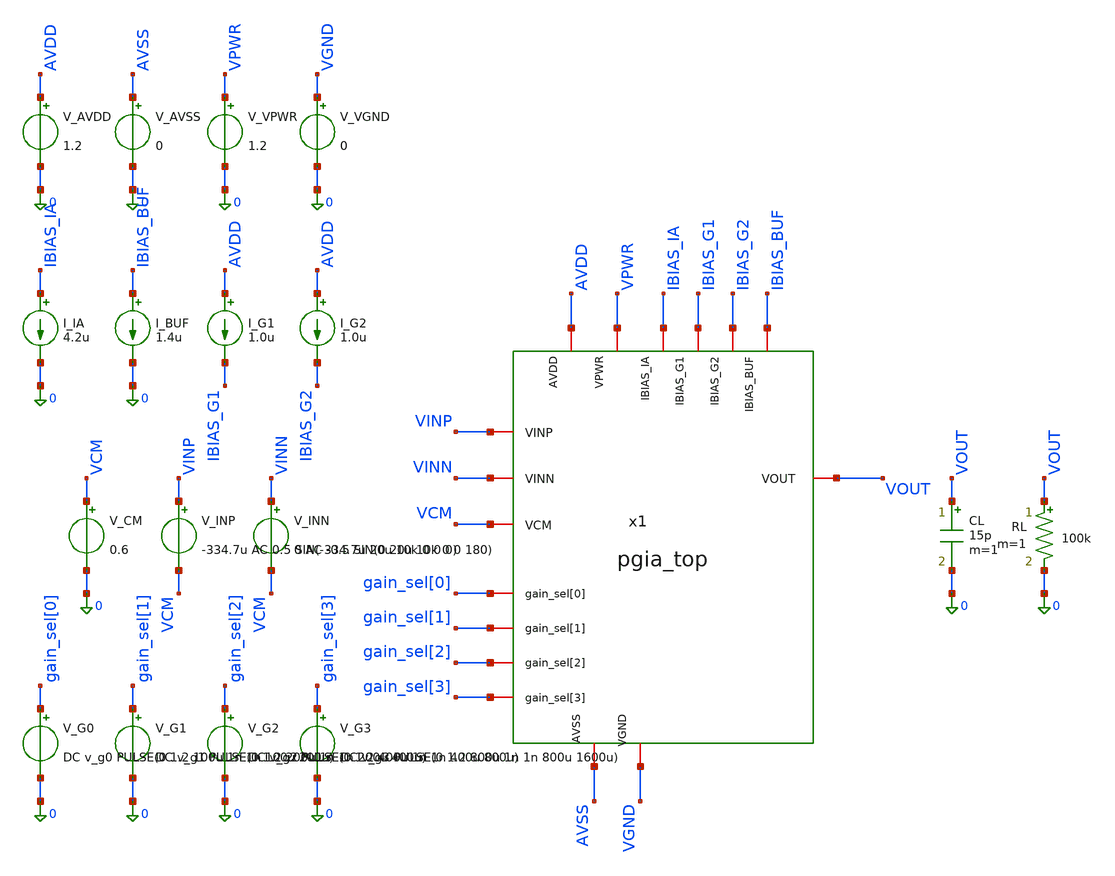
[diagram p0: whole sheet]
** sch_path: xschem/pgia_top/tb_pgia_top.sch
**.subckt tb_pgia_top
x1 VINP VINN VCM gain_sel[0] gain_sel[1] gain_sel[2] gain_sel[3] VOUT AVDD VPWR IBIAS_IA IBIAS_G1
+ IBIAS_G2 IBIAS_BUF AVSS VGND pgia_top
V_AVDD AVDD 0 1.2
V_AVSS AVSS 0 0
V_VPWR VPWR 0 1.2
V_VGND VGND 0 0
I_IA IBIAS_IA 0 4.2u
I_BUF IBIAS_BUF 0 1.4u
I_G1 AVDD IBIAS_G1 1.0u
I_G2 AVDD IBIAS_G2 1.0u
V_CM VCM 0 0.6
V_INP VINP VCM -334.7u AC 0.5 SIN(-334.7u 20u 10k 0 0 0)
V_INN VINN VCM 0 AC -0.5 SIN(0 20u 10k 0 0 180)
V_G0 gain_sel[0] 0 DC v_g0 PULSE(0 1.2 100u 1n 1n 100u 200u)
V_G1 gain_sel[1] 0 DC v_g1 PULSE(0 1.2 200u 1n 1n 200u 400u)
V_G2 gain_sel[2] 0 DC v_g2 PULSE(0 1.2 400u 1n 1n 400u 800u)
V_G3 gain_sel[3] 0 DC v_g3 PULSE(0 1.2 800u 1n 1n 800u 1600u)
CL VOUT 0 15p m=1
RL VOUT 0 100k m=1
**** begin user architecture code


.lib /foss/pdks/ihp-sg13cmos5l/libs.tech/ngspice/models/cornerMOSlv.lib mos_tt
.lib /foss/pdks/ihp-sg13cmos5l/libs.tech/ngspice/models/cornerRES.lib res_typ
.lib /foss/pdks/ihp-sg13cmos5l/libs.tech/ngspice/models/cornerCAP.lib cap_typ
.include /foss/pdks/ihp-sg13cmos5l/libs.ref/sg13cmos5l_stdcell/spice/sg13cmos5l_stdcell.spice
.include /foss/designs/Chipalooza/Programmable-Instrumentation-Amplifier-IP/gds/gain_decoder_4b/final/spice/gain_decoder_4b.spice

.param temp=27
.param lbias=0.15u wbias=0.15u
.param m6=1 m7=4 m8=8
.param linpair=3u winpair=20u
.param lload=5u wload=10u
.param lcs=3u wcs=20u
.param Cc=2p
.param v_g0=0 v_g1=0 v_g2=0 v_g3=0




.control
  save all v(VOUT) v(x1.v_ia) v(x1.v_stage1) v(x1.v_stage2)
  echo ==========================================================================
  echo === TOP-LEVEL PGIA CO-SIMULATION BATTERY (MILESTONES 3, 4, 5) ===
  echo ==========================================================================

  * 1. DC Operating Point Verification
  echo
  echo --- Phase A: DC Operating Point Audit ---
  op
  let v_ia_dc     = v(x1.v_ia)
  let v_st1_dc    = v(x1.v_stage1)
  let v_st2_dc    = v(x1.v_stage2)
  let v_out_dc    = v(VOUT)
  let v_diff_dc   = v(VINP) - v(VINN)
  let i_avdd_dc   = -i(v_avdd)
  let i_vpwr_dc   = -i(v_vpwr)
  let p_tot_uW    = (i_avdd_dc + i_vpwr_dc) * 1.2 * 1e6

  echo Target Common-Mode: 0.600 V
  echo V(VINP) - V(VINN) = $&v_diff_dc V
  echo V(v_ia)           = $&v_ia_dc V
  echo V(v_stage1)       = $&v_st1_dc V
  echo V(v_stage2)       = $&v_st2_dc V
  echo V(VOUT)           = $&v_out_dc V
  echo Total Static DC Power = $&p_tot_uW uW (Target < 500 uW)

  * 2. Small-Signal AC Gain Sweeps Across All 11 Valid Gain Steps (0 to 10)
  echo
  echo --- Phase B: Small-Signal AC Frequency Response (11 Steps) ---

  * Step 0: 0000 (Target: 18.06 dB / 8x)
  alterparam v_g0=0
  alterparam v_g1=0
  alterparam v_g2=0
  alterparam v_g3=0
  reset
  ac dec 10 10 100Meg
  let gain0 = db(v(VOUT))
  let g0_1k = gain0[20]
  echo Step 0  (0000): Gain @ 1kHz = $&g0_1k dB

  * Step 1: 0001 (Target: 24.08 dB / 16x)
  alterparam v_g0=1.2
  alterparam v_g1=0
  alterparam v_g2=0
  alterparam v_g3=0
  reset
  ac dec 10 10 100Meg
  let gain1 = db(v(VOUT))
  let g1_1k = gain1[20]
  echo Step 1  (0001): Gain @ 1kHz = $&g1_1k dB

  * Step 2: 0010 (Target: 30.10 dB / 32x)
  alterparam v_g0=0
  alterparam v_g1=1.2
  alterparam v_g2=0
  alterparam v_g3=0
  reset
  ac dec 10 10 100Meg
  let gain2 = db(v(VOUT))
  let g2_1k = gain2[20]
  echo Step 2  (0010): Gain @ 1kHz = $&g2_1k dB

  * Step 3: 0011 (Target: 36.12 dB / 64x)
  alterparam v_g0=1.2
  alterparam v_g1=1.2
  alterparam v_g2=0
  alterparam v_g3=0
  reset
  ac dec 10 10 100Meg
  let gain3 = db(v(VOUT))
  let g3_1k = gain3[20]
  echo Step 3  (0011): Gain @ 1kHz = $&g3_1k dB

  * Step 4: 0100 (Target: 42.14 dB / 128x)
  alterparam v_g0=0
  alterparam v_g1=0
  alterparam v_g2=1.2
  alterparam v_g3=0
  reset
  ac dec 10 10 100Meg
  let gain4 = db(v(VOUT))
  let g4_1k = gain4[20]
  echo Step 4  (0100): Gain @ 1kHz = $&g4_1k dB

  * Step 5: 0101 (Target: 48.16 dB / 256x)
  alterparam v_g0=1.2
  alterparam v_g1=0
  alterparam v_g2=1.2
  alterparam v_g3=0
  reset
  ac dec 10 10 100Meg
  let gain5 = db(v(VOUT))
  let g5_1k = gain5[20]
  echo Step 5  (0101): Gain @ 1kHz = $&g5_1k dB

  * Step 6: 0110 (Target: 54.18 dB / 512x)
  alterparam v_g0=0
  alterparam v_g1=1.2
  alterparam v_g2=1.2
  alterparam v_g3=0
  reset
  ac dec 10 10 100Meg
  let gain6 = db(v(VOUT))
  let g6_1k = gain6[20]
  echo Step 6  (0110): Gain @ 1kHz = $&g6_1k dB

  * Step 7: 0111 (Target: 60.20 dB / 1024x)
  alterparam v_g0=1.2
  alterparam v_g1=1.2
  alterparam v_g2=1.2
  alterparam v_g3=0
  reset
  ac dec 10 10 100Meg
  let gain7 = db(v(VOUT))
  let g7_1k = gain7[20]
  echo Step 7  (0111): Gain @ 1kHz = $&g7_1k dB

  * Step 8: 1000 (Target: 66.22 dB / 2048x)
  alterparam v_g0=0
  alterparam v_g1=0
  alterparam v_g2=0
  alterparam v_g3=1.2
  reset
  ac dec 10 10 100Meg
  let gain8 = db(v(VOUT))
  let g8_1k = gain8[20]
  echo Step 8  (1000): Gain @ 1kHz = $&g8_1k dB

  * Step 9: 1001 (Target: 72.24 dB / 4096x)
  alterparam v_g0=1.2
  alterparam v_g1=0
  alterparam v_g2=0
  alterparam v_g3=1.2
  reset
  ac dec 10 10 100Meg
  let gain9 = db(v(VOUT))
  let g9_1k = gain9[20]
  echo Step 9  (1001): Gain @ 1kHz = $&g9_1k dB

  * Step 10: 1010 (Target: 78.26 dB / 8192x)
  alterparam v_g0=0
  alterparam v_g1=1.2
  alterparam v_g2=0
  alterparam v_g3=1.2
  reset
  ac dec 10 10 100Meg
  let gain10 = db(v(VOUT))
  let g10_1k = gain10[20]
  echo Step 10 (1010): Gain @ 1kHz = $&g10_1k dB

  * Step 11: 1011 (Out-of-range Clamp Target)
  alterparam v_g0=1.2
  alterparam v_g1=1.2
  alterparam v_g2=0
  alterparam v_g3=1.2
  reset
  ac dec 10 10 100Meg
  let gain11 = db(v(VOUT))
  let g11_1k = gain11[20]
  echo Step 11 (1011): Gain @ 1kHz = $&g11_1k dB (Expected Clamp to Step 0)

  * 3. Dynamic Transient Co-Simulation Across All 16 States (0 to 15)
  echo
  echo --- Phase C: Dynamic Transient Stepping (16 States x 100us) ---
  tran 1u 1.6m
  meas tran vpp_st0  pp v(VOUT) from=50u to=90u
  meas tran vpp_st1  pp v(VOUT) from=150u to=190u
  meas tran vpp_st2  pp v(VOUT) from=250u to=290u
  meas tran vpp_st3  pp v(VOUT) from=350u to=390u
  meas tran vpp_st4  pp v(VOUT) from=450u to=490u
  meas tran vpp_st5  pp v(VOUT) from=550u to=590u
  meas tran vpp_st6  pp v(VOUT) from=650u to=690u
  meas tran vpp_st7  pp v(VOUT) from=750u to=790u
  meas tran vpp_st8  pp v(VOUT) from=850u to=890u
  meas tran vpp_st9  pp v(VOUT) from=950u to=990u
  meas tran vpp_st10 pp v(VOUT) from=1050u to=1090u
  meas tran vpp_st11 pp v(VOUT) from=1150u to=1190u
  meas tran vpp_st12 pp v(VOUT) from=1250u to=1290u
  meas tran vpp_st15 pp v(VOUT) from=1550u to=1590u

  echo
  echo Transient Output Peak-to-Peak:
  echo State 0  (0000): $&vpp_st0 Vpp
  echo State 1  (0001): $&vpp_st1 Vpp
  echo State 2  (0010): $&vpp_st2 Vpp
  echo State 3  (0011): $&vpp_st3 Vpp
  echo State 4  (0100): $&vpp_st4 Vpp
  echo State 5  (0101): $&vpp_st5 Vpp
  echo State 6  (0110): $&vpp_st6 Vpp
  echo State 7  (0111): $&vpp_st7 Vpp
  echo State 8  (1000): $&vpp_st8 Vpp
  echo State 9  (1001): $&vpp_st9 Vpp
  echo State 10 (1010): $&vpp_st10 Vpp
  echo State 11 (1011): $&vpp_st11 Vpp (Clamped)
  echo State 12 (1100): $&vpp_st12 Vpp (Clamped)
  echo State 15 (1111): $&vpp_st15 Vpp (Clamped)

  echo ==========================================================================
  echo === SIMULATION COMPLETE ===
  echo ==========================================================================
.endc


**** end user architecture code
**.ends
.end
